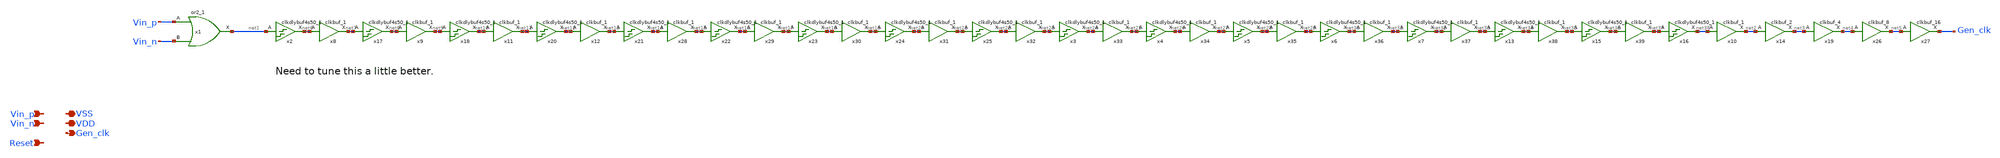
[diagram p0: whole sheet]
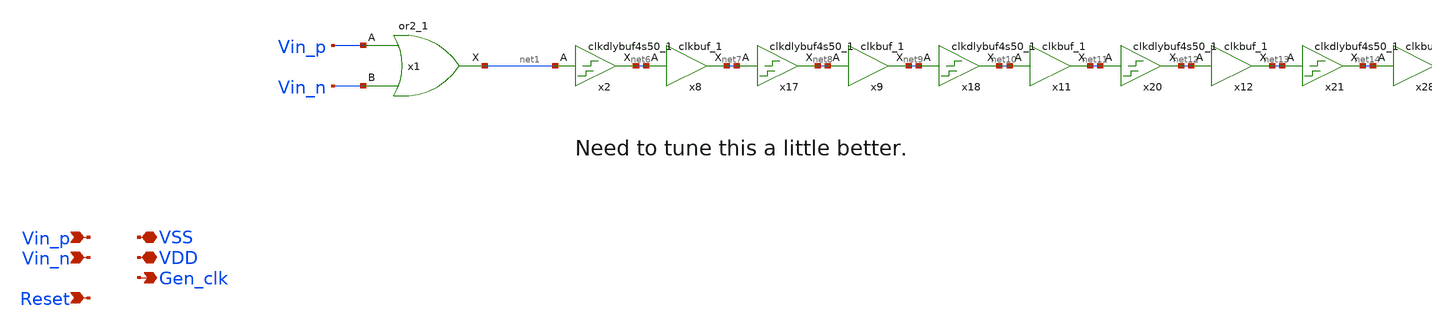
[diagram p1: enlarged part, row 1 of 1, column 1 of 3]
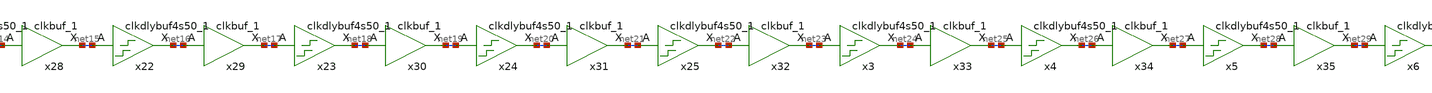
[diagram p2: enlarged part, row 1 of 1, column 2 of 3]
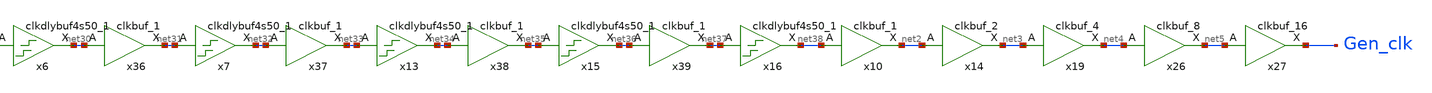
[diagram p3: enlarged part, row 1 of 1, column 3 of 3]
** sch_path: xschem/src/xor_clock_gen/xor_clock_gen_w_single_bufs.sch
**.subckt xor_clock_gen_w_single_bufs Vin_p VSS Gen_clk VDD Vin_n Reset
*.ipin Vin_p
*.iopin VSS
*.opin Gen_clk
*.iopin VDD
*.ipin Vin_n
*.ipin Reset
x2 net1 VSS VSS VDD VDD net6 sky130_fd_sc_hd__clkdlybuf4s50_1
x3 net23 VSS VSS VDD VDD net24 sky130_fd_sc_hd__clkdlybuf4s50_1
x4 net25 VSS VSS VDD VDD net26 sky130_fd_sc_hd__clkdlybuf4s50_1
x5 net27 VSS VSS VDD VDD net28 sky130_fd_sc_hd__clkdlybuf4s50_1
x6 net29 VSS VSS VDD VDD net30 sky130_fd_sc_hd__clkdlybuf4s50_1
x7 net31 VSS VSS VDD VDD net32 sky130_fd_sc_hd__clkdlybuf4s50_1
x13 net33 VSS VSS VDD VDD net34 sky130_fd_sc_hd__clkdlybuf4s50_1
x15 net35 VSS VSS VDD VDD net36 sky130_fd_sc_hd__clkdlybuf4s50_1
x16 net37 VSS VSS VDD VDD net38 sky130_fd_sc_hd__clkdlybuf4s50_1
x17 net7 VSS VSS VDD VDD net8 sky130_fd_sc_hd__clkdlybuf4s50_1
x18 net9 VSS VSS VDD VDD net10 sky130_fd_sc_hd__clkdlybuf4s50_1
x20 net11 VSS VSS VDD VDD net12 sky130_fd_sc_hd__clkdlybuf4s50_1
x21 net13 VSS VSS VDD VDD net14 sky130_fd_sc_hd__clkdlybuf4s50_1
x22 net15 VSS VSS VDD VDD net16 sky130_fd_sc_hd__clkdlybuf4s50_1
x23 net17 VSS VSS VDD VDD net18 sky130_fd_sc_hd__clkdlybuf4s50_1
x24 net19 VSS VSS VDD VDD net20 sky130_fd_sc_hd__clkdlybuf4s50_1
x25 net21 VSS VSS VDD VDD net22 sky130_fd_sc_hd__clkdlybuf4s50_1
x10 net38 VSS VSS VDD VDD net2 sky130_fd_sc_hd__clkbuf_1
x14 net2 VSS VSS VDD VDD net3 sky130_fd_sc_hd__clkbuf_2
x19 net3 VSS VSS VDD VDD net4 sky130_fd_sc_hd__clkbuf_4
x26 net4 VSS VSS VDD VDD net5 sky130_fd_sc_hd__clkbuf_8
x27 net5 VSS VSS VDD VDD Gen_clk sky130_fd_sc_hd__clkbuf_16
x8 net6 VSS VSS VDD VDD net7 sky130_fd_sc_hd__clkbuf_1
x9 net8 VSS VSS VDD VDD net9 sky130_fd_sc_hd__clkbuf_1
x11 net10 VSS VSS VDD VDD net11 sky130_fd_sc_hd__clkbuf_1
x12 net12 VSS VSS VDD VDD net13 sky130_fd_sc_hd__clkbuf_1
x28 net14 VSS VSS VDD VDD net15 sky130_fd_sc_hd__clkbuf_1
x29 net16 VSS VSS VDD VDD net17 sky130_fd_sc_hd__clkbuf_1
x30 net18 VSS VSS VDD VDD net19 sky130_fd_sc_hd__clkbuf_1
x31 net20 VSS VSS VDD VDD net21 sky130_fd_sc_hd__clkbuf_1
x32 net22 VSS VSS VDD VDD net23 sky130_fd_sc_hd__clkbuf_1
x33 net24 VSS VSS VDD VDD net25 sky130_fd_sc_hd__clkbuf_1
x34 net26 VSS VSS VDD VDD net27 sky130_fd_sc_hd__clkbuf_1
x35 net28 VSS VSS VDD VDD net29 sky130_fd_sc_hd__clkbuf_1
x36 net30 VSS VSS VDD VDD net31 sky130_fd_sc_hd__clkbuf_1
x37 net32 VSS VSS VDD VDD net33 sky130_fd_sc_hd__clkbuf_1
x38 net34 VSS VSS VDD VDD net35 sky130_fd_sc_hd__clkbuf_1
x39 net36 VSS VSS VDD VDD net37 sky130_fd_sc_hd__clkbuf_1
x1 Vin_p Vin_n VSS VSS VDD VDD net1 sky130_fd_sc_hd__or2_1
**.ends
.end
